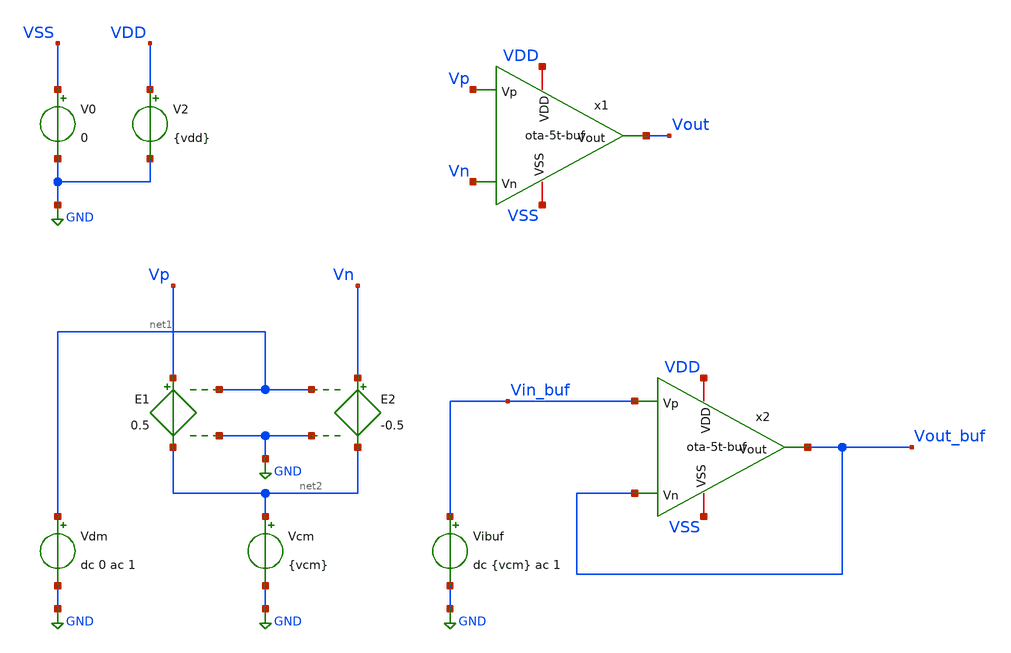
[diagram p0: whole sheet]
** sch_path: ota-5t-buf/xschem/ota-5t-buf_tb.sch
**.subckt ota-5t-buf_tb
x1 Vp Vn Vout VDD VSS ota-5t-buf
V0 VSS GND 0
V2 VDD GND {vdd}
E1 Vp net2 net1 GND 0.5
E2 Vn net2 net1 GND -0.5
Vdm net1 GND dc 0 ac 1
Vcm net2 GND {vcm}
x2 Vin_buf Vout_buf Vout_buf VDD VSS ota-5t-buf
Vibuf Vin_buf GND dc {vcm} ac 1
**** begin user architecture code


.param vdd=1.8
.param vcm=0.9
.include ../sizing_ota-5t-buf.spice
.lib /foss/pdks/sky130A/libs.tech/ngspice/sky130.lib.spice tt

.control
    save all
    save @m.x1.xm2a.msky130_fd_pr__pfet_01v8[id] @m.x1.xm2a.msky130_fd_pr__pfet_01v8[gm]
+ @m.x1.xm2a.msky130_fd_pr__pfet_01v8[gds]
    save @m.x1.xm2b.msky130_fd_pr__pfet_01v8[id] @m.x1.xm2b.msky130_fd_pr__pfet_01v8[gm]
+ @m.x1.xm2b.msky130_fd_pr__pfet_01v8[gds]
    save @m.x1.xm1a.msky130_fd_pr__nfet_01v8_lvt[id] @m.x1.xm1a.msky130_fd_pr__nfet_01v8_lvt[gm]
+ @m.x1.xm1a.msky130_fd_pr__nfet_01v8_lvt[gds]
    save @m.x1.xm1b.msky130_fd_pr__nfet_01v8_lvt[id] @m.x1.xm1b.msky130_fd_pr__nfet_01v8_lvt[gm]
+ @m.x1.xm1b.msky130_fd_pr__nfet_01v8_lvt[gds]
    save @m.x1.xm0a.msky130_fd_pr__nfet_01v8_lvt[id] @m.x1.xm0a.msky130_fd_pr__nfet_01v8_lvt[gm]
+ @m.x1.xm0a.msky130_fd_pr__nfet_01v8_lvt[gds]
    save @m.x1.xm0b.msky130_fd_pr__nfet_01v8_lvt[id] @m.x1.xm0b.msky130_fd_pr__nfet_01v8_lvt[gm]
+ @m.x1.xm0b.msky130_fd_pr__nfet_01v8_lvt[gds]

    op
    show

    noise v(Vout_buf) Vibuf dec 20 1k 100e9
    setplot noise2
    print onoise_total
    let NOI = onoise_total/1e-6
    echo $&NOI
    write ota-5t-buf_tb_noise2.raw noise2.all

    ac dec 20 1k 100e9
    let vout_mag = abs(v(Vout))
    let vout_phase_margin = phase(v(Vout)) * 180/pi + 180
    meas ac A0 find vout_mag at=1k
    meas ac UGF when vout_mag=1 fall=1
    meas ac PM find vout_phase_margin when vout_mag=1
    echo $&A0 $&UGF $&PM
    echo $plots
    write ota-5t-buf_tb.raw op1.all noise1.all ac2.all
.endc


**** end user architecture code
**.ends
.GLOBAL GND
.end
